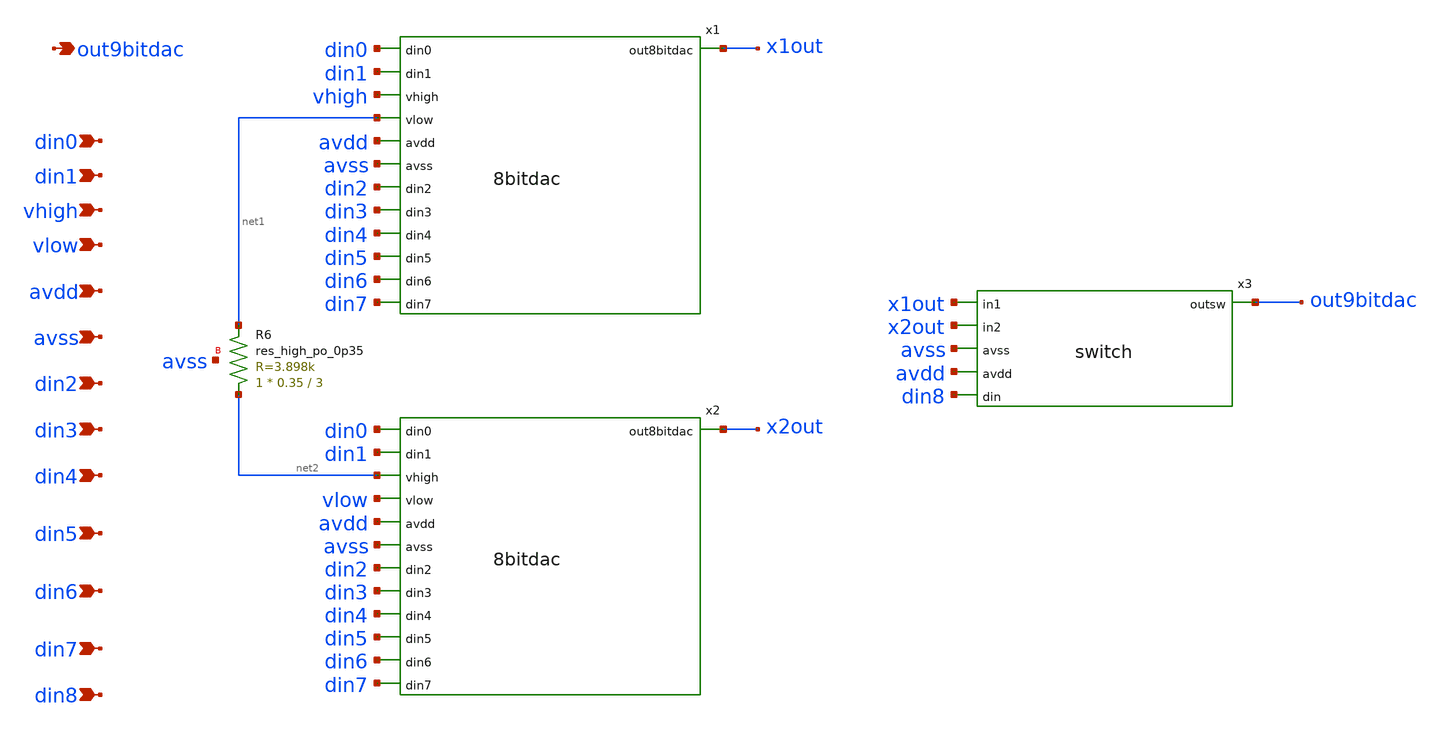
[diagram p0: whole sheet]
** sch_path: xschem/9bitdac.sch
**.subckt 9bitdac din0 din1 vhigh vlow avdd avss din2 din3 out9bitdac din4 din5 din6 din7 din8
*.ipin din0
*.ipin din1
*.ipin vhigh
*.ipin vlow
*.ipin avdd
*.ipin avss
*.ipin din2
*.ipin din3
*.opin out9bitdac
*.ipin din4
*.ipin din5
*.ipin din6
*.ipin din7
*.ipin din8
x1 x1out din0 din1 vhigh net1 avdd avss din2 din3 din4 din5 din6 din7 8bitdac
x2 x2out din0 din1 net2 vlow avdd avss din2 din3 din4 din5 din6 din7 8bitdac
x3 out9bitdac x1out x2out avss avdd din8 switch
XR6 net2 net1 avss sky130_fd_pr__res_high_po_0p35 L=3 mult=1 m=1
**.ends
.end
